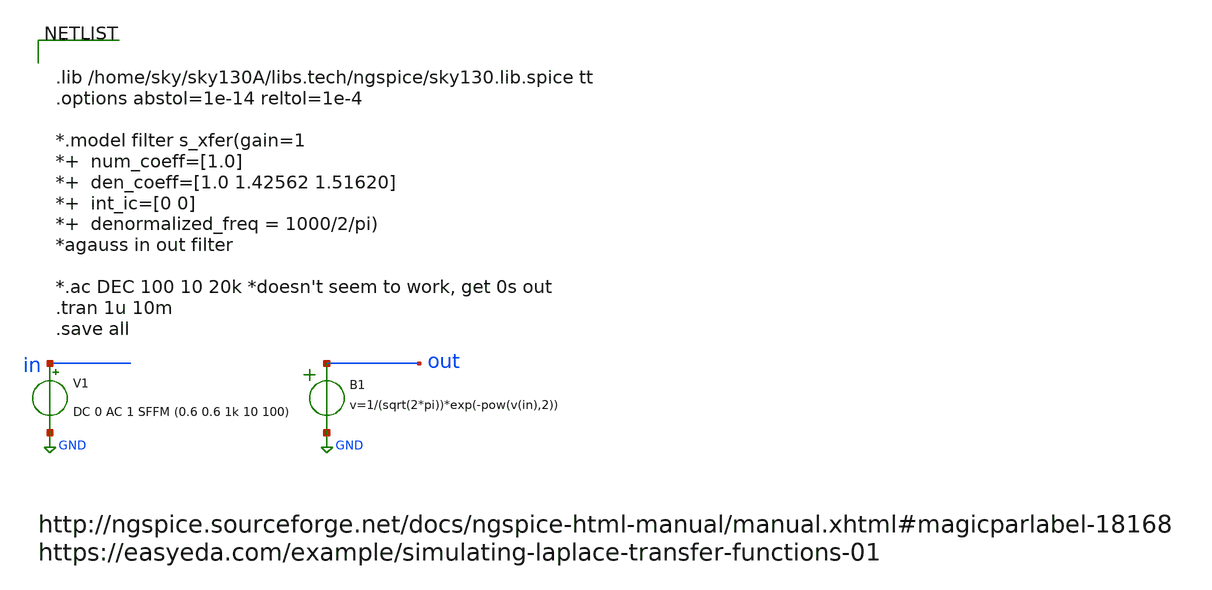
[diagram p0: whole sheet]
** sch_path: xschem/Switched_Caps/vcvs_gaussian_tb.sch
**.subckt vcvs_gaussian_tb
V1 in GND DC 0 AC 1 SFFM (0.6 0.6 1k 10 100)
B1 out GND v=1/(sqrt(2*pi))*exp(-pow(v(in),2))
**** begin user architecture code


.lib /home/sky/sky130A/libs.tech/ngspice/sky130.lib.spice tt
.options abstol=1e-14 reltol=1e-4

*.model filter s_xfer(gain=1
*+  num_coeff=[1.0]
*+  den_coeff=[1.0 1.42562 1.51620]
*+  int_ic=[0 0]
*+  denormalized_freq = 1000/2/pi)
*agauss in out filter

*.ac DEC 100 10 20k *doesn't seem to work, get 0s out
.tran 1u 10m
.save all


**** end user architecture code
**.ends
.GLOBAL GND
.end
